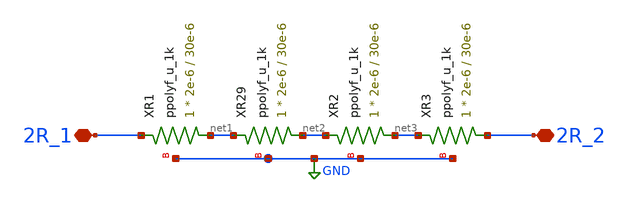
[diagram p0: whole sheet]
** sch_path: xschem/2R.sch
**.subckt 2R 2R_1 2R_2
*.iopin 2R_1
*.iopin 2R_2
XR1 net1 2R_1 GND ppolyf_u_1k r_width=2e-6 r_length=30e-6 m=1
XR29 net2 net1 GND ppolyf_u_1k r_width=2e-6 r_length=30e-6 m=1
XR2 net3 net2 GND ppolyf_u_1k r_width=2e-6 r_length=30e-6 m=1
XR3 2R_2 net3 GND ppolyf_u_1k r_width=2e-6 r_length=30e-6 m=1
**.ends
.GLOBAL GND
.end
